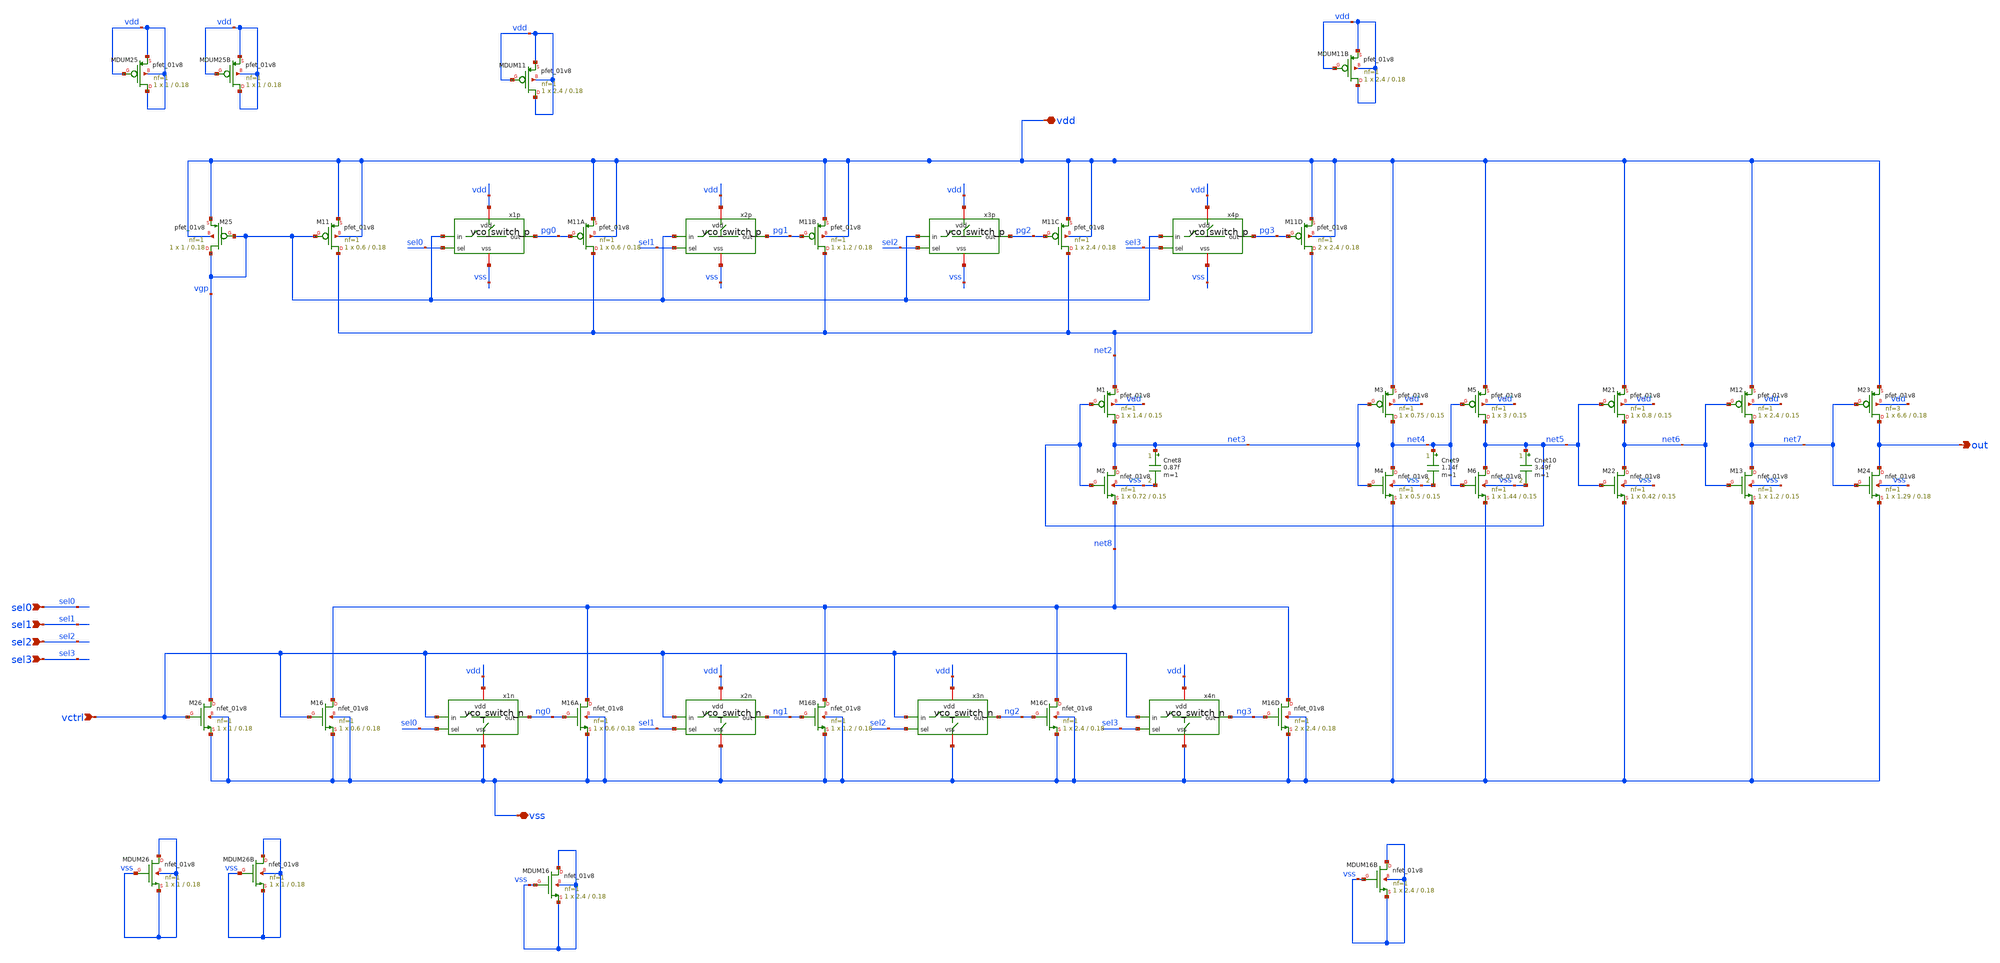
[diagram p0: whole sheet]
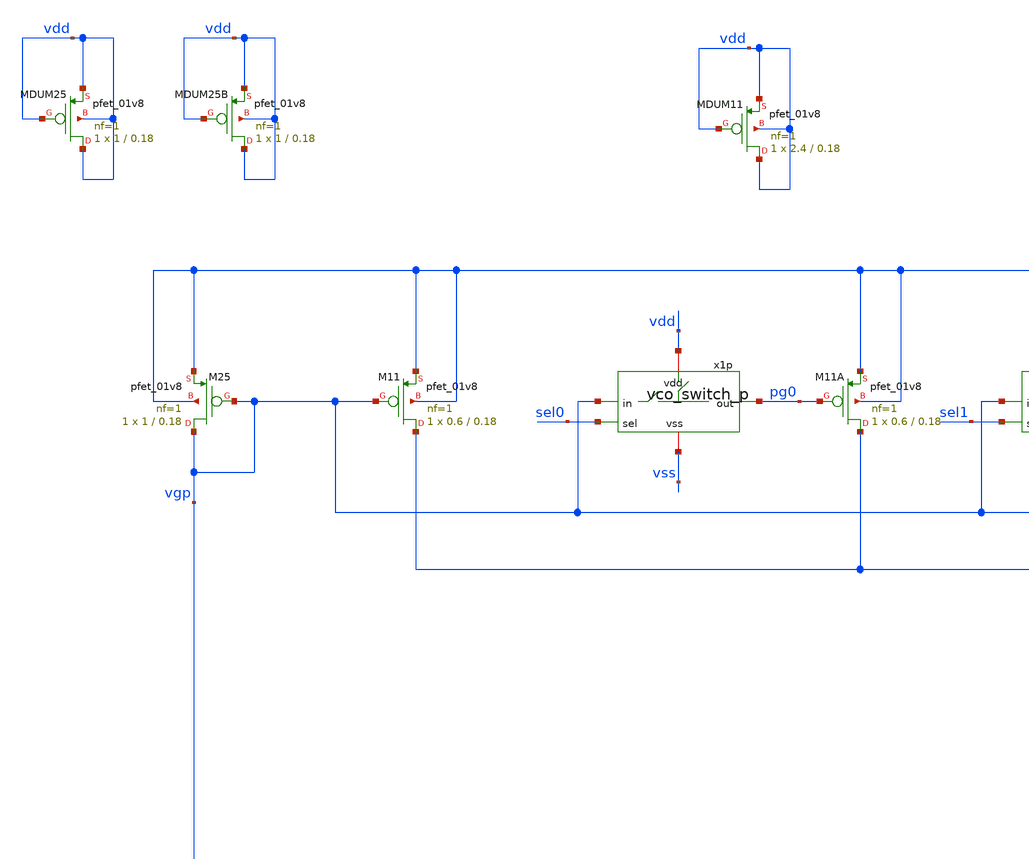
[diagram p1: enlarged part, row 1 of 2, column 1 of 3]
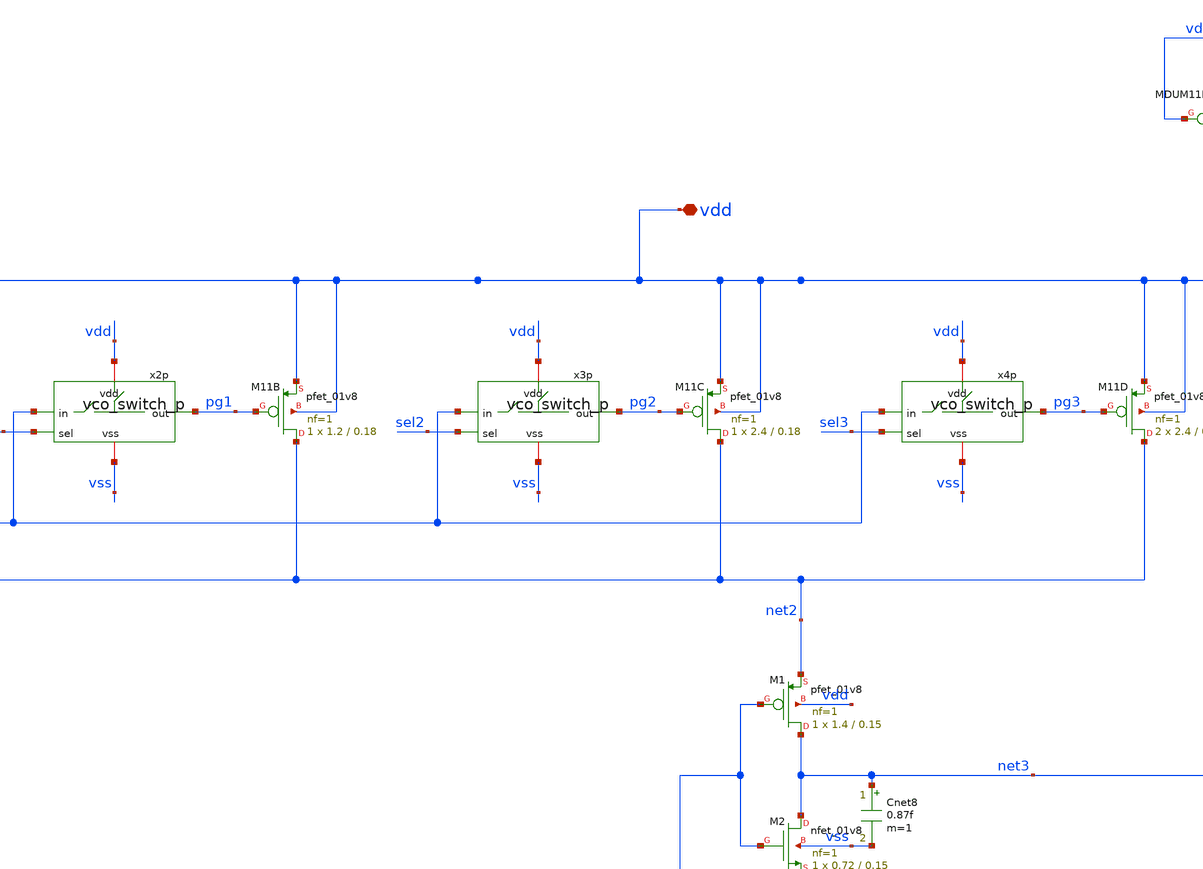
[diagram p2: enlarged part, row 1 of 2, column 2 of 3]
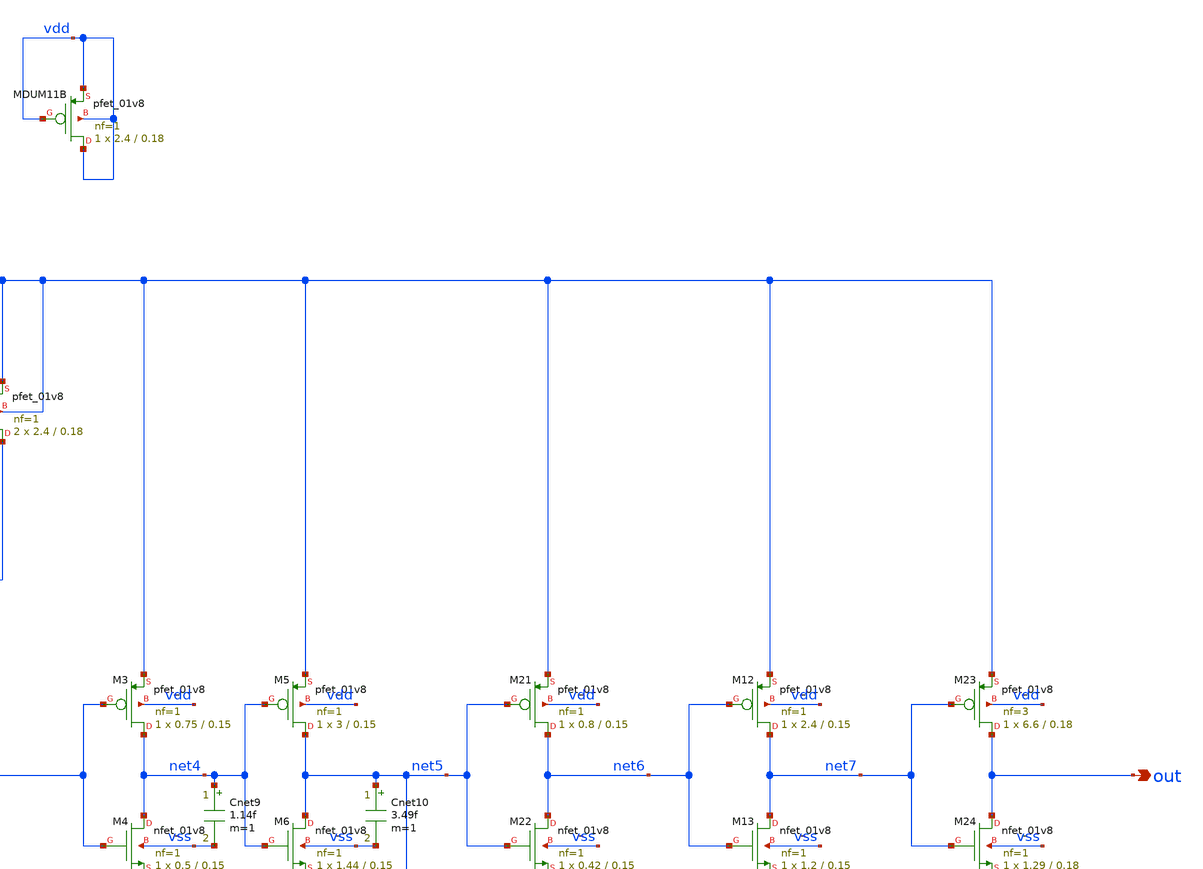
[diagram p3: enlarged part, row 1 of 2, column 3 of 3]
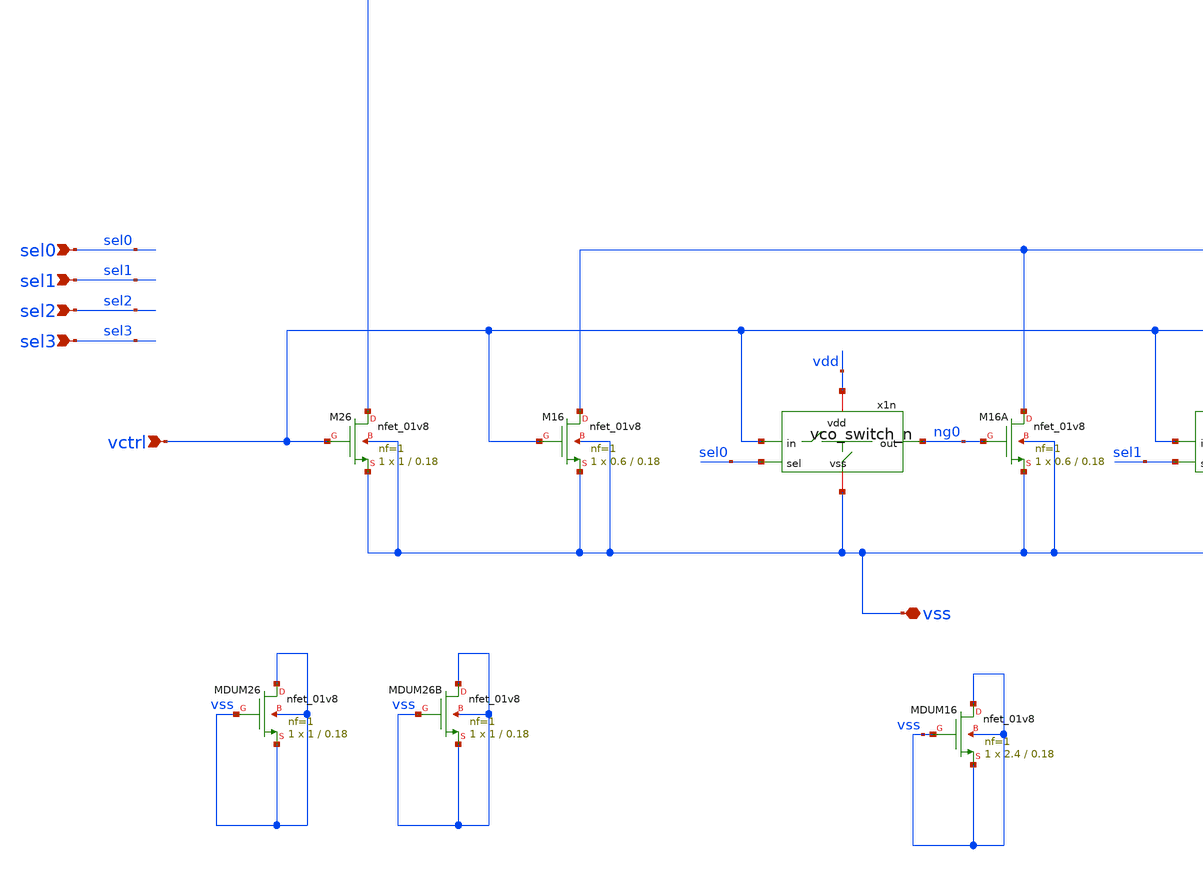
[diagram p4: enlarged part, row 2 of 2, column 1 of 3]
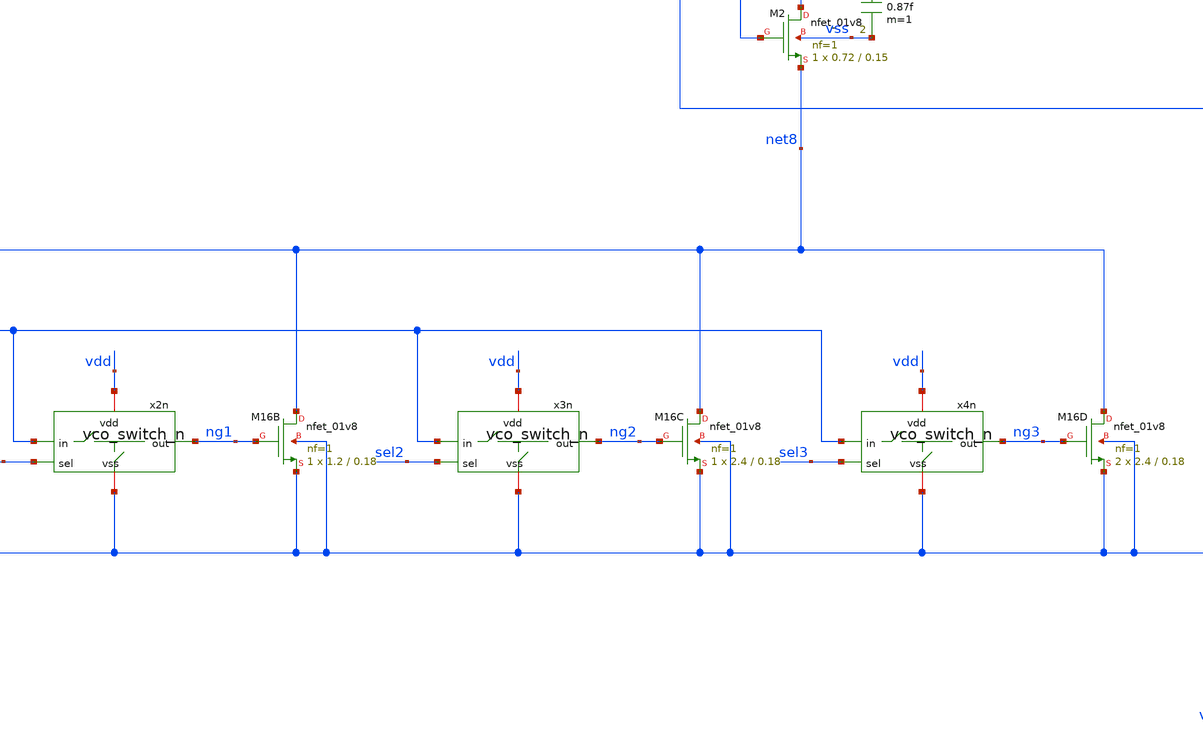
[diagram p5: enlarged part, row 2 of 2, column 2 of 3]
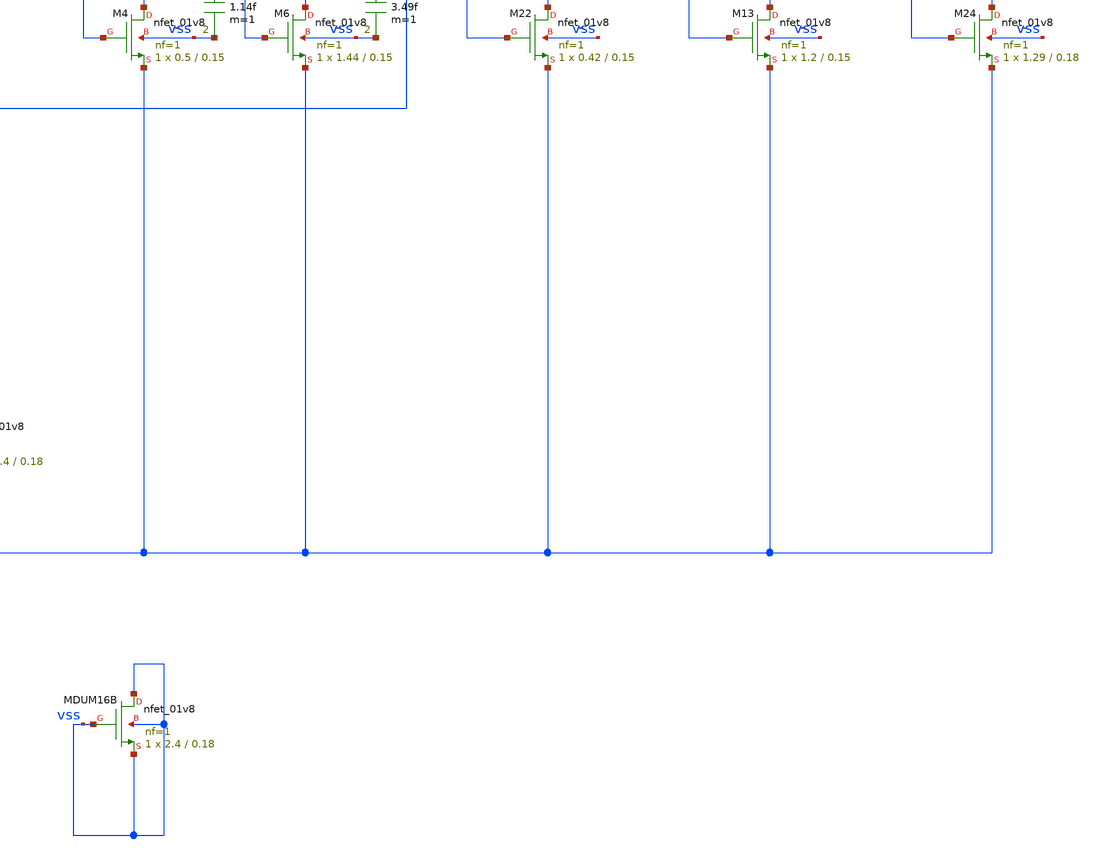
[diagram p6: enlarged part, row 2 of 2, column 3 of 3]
** sch_path: xschem/3-stage_cs-vco_dp9/3-stage_cs-vco_dp9.sch
**.subckt 3-stage_cs-vco_dp9 vdd vss out vctrl sel0 sel1 sel2 sel3
*.iopin vdd
*.iopin vss
*.opin out
*.ipin vctrl
*.ipin sel0
*.ipin sel1
*.ipin sel2
*.ipin sel3
XM25 vgp vgp vdd vdd sky130_fd_pr__pfet_01v8 L=0.18 W=1 nf=1 ad='int((nf+1)/2) * W/nf * 0.29' as='int((nf+2)/2) * W/nf * 0.29'
+ pd='2*int((nf+1)/2) * (W/nf + 0.29)' ps='2*int((nf+2)/2) * (W/nf + 0.29)' nrd='0.29 / W' nrs='0.29 / W'
+ sa=0 sb=0 sd=0 mult=1 m=1
XM26 vgp vctrl vss vss sky130_fd_pr__nfet_01v8 L=0.18 W=1 nf=1 ad='int((nf+1)/2) * W/nf * 0.29' as='int((nf+2)/2) * W/nf * 0.29'
+ pd='2*int((nf+1)/2) * (W/nf + 0.29)' ps='2*int((nf+2)/2) * (W/nf + 0.29)' nrd='0.29 / W' nrs='0.29 / W'
+ sa=0 sb=0 sd=0 mult=1 m=1
XM11C net2 pg2 vdd vdd sky130_fd_pr__pfet_01v8 L=0.18 W=2.4 nf=1 ad='int((nf+1)/2) * W/nf * 0.29' as='int((nf+2)/2) * W/nf * 0.29'
+ pd='2*int((nf+1)/2) * (W/nf + 0.29)' ps='2*int((nf+2)/2) * (W/nf + 0.29)' nrd='0.29 / W' nrs='0.29 / W'
+ sa=0 sb=0 sd=0 mult=1 m=1
XM16A net8 ng0 vss vss sky130_fd_pr__nfet_01v8 L=0.18 W=0.6 nf=1 ad='int((nf+1)/2) * W/nf * 0.29' as='int((nf+2)/2) * W/nf * 0.29'
+ pd='2*int((nf+1)/2) * (W/nf + 0.29)' ps='2*int((nf+2)/2) * (W/nf + 0.29)' nrd='0.29 / W' nrs='0.29 / W'
+ sa=0 sb=0 sd=0 mult=1 m=1
XM1 net3 net5 net2 vdd sky130_fd_pr__pfet_01v8 L=0.15 W=1.4 nf=1 ad='int((nf+1)/2) * W/nf * 0.29' as='int((nf+2)/2) * W/nf * 0.29'
+ pd='2*int((nf+1)/2) * (W/nf + 0.29)' ps='2*int((nf+2)/2) * (W/nf + 0.29)' nrd='0.29 / W' nrs='0.29 / W'
+ sa=0 sb=0 sd=0 mult=1 m=1
XM3 net4 net3 vdd vdd sky130_fd_pr__pfet_01v8 L=0.15 W=0.75 nf=1 ad='int((nf+1)/2) * W/nf * 0.29' as='int((nf+2)/2) * W/nf * 0.29'
+ pd='2*int((nf+1)/2) * (W/nf + 0.29)' ps='2*int((nf+2)/2) * (W/nf + 0.29)' nrd='0.29 / W' nrs='0.29 / W'
+ sa=0 sb=0 sd=0 mult=1 m=1
XM5 net5 net4 vdd vdd sky130_fd_pr__pfet_01v8 L=0.15 W=3 nf=1 ad='int((nf+1)/2) * W/nf * 0.29' as='int((nf+2)/2) * W/nf * 0.29'
+ pd='2*int((nf+1)/2) * (W/nf + 0.29)' ps='2*int((nf+2)/2) * (W/nf + 0.29)' nrd='0.29 / W' nrs='0.29 / W'
+ sa=0 sb=0 sd=0 mult=1 m=1
XM2 net3 net5 net8 vss sky130_fd_pr__nfet_01v8 L=0.15 W=0.72 nf=1 ad='int((nf+1)/2) * W/nf * 0.29' as='int((nf+2)/2) * W/nf * 0.29'
+ pd='2*int((nf+1)/2) * (W/nf + 0.29)' ps='2*int((nf+2)/2) * (W/nf + 0.29)' nrd='0.29 / W' nrs='0.29 / W'
+ sa=0 sb=0 sd=0 mult=1 m=1
XM4 net4 net3 vss vss sky130_fd_pr__nfet_01v8 L=0.15 W=0.5 nf=1 ad='int((nf+1)/2) * W/nf * 0.29' as='int((nf+2)/2) * W/nf * 0.29'
+ pd='2*int((nf+1)/2) * (W/nf + 0.29)' ps='2*int((nf+2)/2) * (W/nf + 0.29)' nrd='0.29 / W' nrs='0.29 / W'
+ sa=0 sb=0 sd=0 mult=1 m=1
XM6 net5 net4 vss vss sky130_fd_pr__nfet_01v8 L=0.15 W=1.44 nf=1 ad='int((nf+1)/2) * W/nf * 0.29' as='int((nf+2)/2) * W/nf * 0.29'
+ pd='2*int((nf+1)/2) * (W/nf + 0.29)' ps='2*int((nf+2)/2) * (W/nf + 0.29)' nrd='0.29 / W' nrs='0.29 / W'
+ sa=0 sb=0 sd=0 mult=1 m=1
XM21 net6 net5 vdd vdd sky130_fd_pr__pfet_01v8 L=0.15 W=0.8 nf=1 ad='int((nf+1)/2) * W/nf * 0.29' as='int((nf+2)/2) * W/nf * 0.29'
+ pd='2*int((nf+1)/2) * (W/nf + 0.29)' ps='2*int((nf+2)/2) * (W/nf + 0.29)' nrd='0.29 / W' nrs='0.29 / W'
+ sa=0 sb=0 sd=0 mult=1 m=1
XM22 net6 net5 vss vss sky130_fd_pr__nfet_01v8 L=0.15 W=0.42 nf=1 ad='int((nf+1)/2) * W/nf * 0.29' as='int((nf+2)/2) * W/nf * 0.29'
+ pd='2*int((nf+1)/2) * (W/nf + 0.29)' ps='2*int((nf+2)/2) * (W/nf + 0.29)' nrd='0.29 / W' nrs='0.29 / W'
+ sa=0 sb=0 sd=0 mult=1 m=1
XM23 out net7 vdd vdd sky130_fd_pr__pfet_01v8 L=0.18 W=6.6 nf=3 ad='int((nf+1)/2) * W/nf * 0.29' as='int((nf+2)/2) * W/nf * 0.29'
+ pd='2*int((nf+1)/2) * (W/nf + 0.29)' ps='2*int((nf+2)/2) * (W/nf + 0.29)' nrd='0.29 / W' nrs='0.29 / W'
+ sa=0 sb=0 sd=0 mult=1 m=1
XM24 out net7 vss vss sky130_fd_pr__nfet_01v8 L=0.18 W=1.29 nf=1 ad='int((nf+1)/2) * W/nf * 0.29' as='int((nf+2)/2) * W/nf * 0.29'
+ pd='2*int((nf+1)/2) * (W/nf + 0.29)' ps='2*int((nf+2)/2) * (W/nf + 0.29)' nrd='0.29 / W' nrs='0.29 / W'
+ sa=0 sb=0 sd=0 mult=1 m=1
XM12 net7 net6 vdd vdd sky130_fd_pr__pfet_01v8 L=0.15 W=2.4 nf=1 ad='int((nf+1)/2) * W/nf * 0.29' as='int((nf+2)/2) * W/nf * 0.29'
+ pd='2*int((nf+1)/2) * (W/nf + 0.29)' ps='2*int((nf+2)/2) * (W/nf + 0.29)' nrd='0.29 / W' nrs='0.29 / W'
+ sa=0 sb=0 sd=0 mult=1 m=1
XM13 net7 net6 vss vss sky130_fd_pr__nfet_01v8 L=0.15 W=1.2 nf=1 ad='int((nf+1)/2) * W/nf * 0.29' as='int((nf+2)/2) * W/nf * 0.29'
+ pd='2*int((nf+1)/2) * (W/nf + 0.29)' ps='2*int((nf+2)/2) * (W/nf + 0.29)' nrd='0.29 / W' nrs='0.29 / W'
+ sa=0 sb=0 sd=0 mult=1 m=1
XMDUM16B vss vss vss vss sky130_fd_pr__nfet_01v8 L=0.18 W=2.4 nf=1 ad='int((nf+1)/2) * W/nf * 0.29' as='int((nf+2)/2) * W/nf * 0.29'
+ pd='2*int((nf+1)/2) * (W/nf + 0.29)' ps='2*int((nf+2)/2) * (W/nf + 0.29)' nrd='0.29 / W' nrs='0.29 / W'
+ sa=0 sb=0 sd=0 mult=1 m=1
XMDUM16 vss vss vss vss sky130_fd_pr__nfet_01v8 L=0.18 W=2.4 nf=1 ad='int((nf+1)/2) * W/nf * 0.29' as='int((nf+2)/2) * W/nf * 0.29'
+ pd='2*int((nf+1)/2) * (W/nf + 0.29)' ps='2*int((nf+2)/2) * (W/nf + 0.29)' nrd='0.29 / W' nrs='0.29 / W'
+ sa=0 sb=0 sd=0 mult=1 m=1
XMDUM26 vss vss vss vss sky130_fd_pr__nfet_01v8 L=0.18 W=1 nf=1 ad='int((nf+1)/2) * W/nf * 0.29' as='int((nf+2)/2) * W/nf * 0.29'
+ pd='2*int((nf+1)/2) * (W/nf + 0.29)' ps='2*int((nf+2)/2) * (W/nf + 0.29)' nrd='0.29 / W' nrs='0.29 / W'
+ sa=0 sb=0 sd=0 mult=1 m=1
XMDUM11B vdd vdd vdd vdd sky130_fd_pr__pfet_01v8 L=0.18 W=2.4 nf=1 ad='int((nf+1)/2) * W/nf * 0.29' as='int((nf+2)/2) * W/nf * 0.29'
+ pd='2*int((nf+1)/2) * (W/nf + 0.29)' ps='2*int((nf+2)/2) * (W/nf + 0.29)' nrd='0.29 / W' nrs='0.29 / W'
+ sa=0 sb=0 sd=0 mult=1 m=1
XMDUM11 vdd vdd vdd vdd sky130_fd_pr__pfet_01v8 L=0.18 W=2.4 nf=1 ad='int((nf+1)/2) * W/nf * 0.29' as='int((nf+2)/2) * W/nf * 0.29'
+ pd='2*int((nf+1)/2) * (W/nf + 0.29)' ps='2*int((nf+2)/2) * (W/nf + 0.29)' nrd='0.29 / W' nrs='0.29 / W'
+ sa=0 sb=0 sd=0 mult=1 m=1
XMDUM25 vdd vdd vdd vdd sky130_fd_pr__pfet_01v8 L=0.18 W=1 nf=1 ad='int((nf+1)/2) * W/nf * 0.29' as='int((nf+2)/2) * W/nf * 0.29'
+ pd='2*int((nf+1)/2) * (W/nf + 0.29)' ps='2*int((nf+2)/2) * (W/nf + 0.29)' nrd='0.29 / W' nrs='0.29 / W'
+ sa=0 sb=0 sd=0 mult=1 m=1
Cnet8 net3 vss 0.87f m=1
Cnet9 net4 vss 1.14f m=1
Cnet10 net5 vss 3.49f m=1
XMDUM26B vss vss vss vss sky130_fd_pr__nfet_01v8 L=0.18 W=1 nf=1 ad='int((nf+1)/2) * W/nf * 0.29' as='int((nf+2)/2) * W/nf * 0.29'
+ pd='2*int((nf+1)/2) * (W/nf + 0.29)' ps='2*int((nf+2)/2) * (W/nf + 0.29)' nrd='0.29 / W' nrs='0.29 / W'
+ sa=0 sb=0 sd=0 mult=1 m=1
XMDUM25B vdd vdd vdd vdd sky130_fd_pr__pfet_01v8 L=0.18 W=1 nf=1 ad='int((nf+1)/2) * W/nf * 0.29' as='int((nf+2)/2) * W/nf * 0.29'
+ pd='2*int((nf+1)/2) * (W/nf + 0.29)' ps='2*int((nf+2)/2) * (W/nf + 0.29)' nrd='0.29 / W' nrs='0.29 / W'
+ sa=0 sb=0 sd=0 mult=1 m=1
x1n vdd ng0 vctrl vss sel0 vco_switch_n
XM16B net8 ng1 vss vss sky130_fd_pr__nfet_01v8 L=0.18 W=1.2 nf=1 ad='int((nf+1)/2) * W/nf * 0.29' as='int((nf+2)/2) * W/nf * 0.29'
+ pd='2*int((nf+1)/2) * (W/nf + 0.29)' ps='2*int((nf+2)/2) * (W/nf + 0.29)' nrd='0.29 / W' nrs='0.29 / W'
+ sa=0 sb=0 sd=0 mult=1 m=1
x2n vdd ng1 vctrl vss sel1 vco_switch_n
XM16C net8 ng2 vss vss sky130_fd_pr__nfet_01v8 L=0.18 W=2.4 nf=1 ad='int((nf+1)/2) * W/nf * 0.29' as='int((nf+2)/2) * W/nf * 0.29'
+ pd='2*int((nf+1)/2) * (W/nf + 0.29)' ps='2*int((nf+2)/2) * (W/nf + 0.29)' nrd='0.29 / W' nrs='0.29 / W'
+ sa=0 sb=0 sd=0 mult=1 m=1
x3n vdd ng2 vctrl vss sel2 vco_switch_n
XM16D net8 ng3 vss vss sky130_fd_pr__nfet_01v8 L=0.18 W=2.4 nf=1 ad='int((nf+1)/2) * W/nf * 0.29' as='int((nf+2)/2) * W/nf * 0.29'
+ pd='2*int((nf+1)/2) * (W/nf + 0.29)' ps='2*int((nf+2)/2) * (W/nf + 0.29)' nrd='0.29 / W' nrs='0.29 / W'
+ sa=0 sb=0 sd=0 mult=2 m=2
x4n vdd ng3 vctrl vss sel3 vco_switch_n
x3p vdd pg2 vgp vss sel2 vco_switch_p
XM11D net2 pg3 vdd vdd sky130_fd_pr__pfet_01v8 L=0.18 W=2.4 nf=1 ad='int((nf+1)/2) * W/nf * 0.29' as='int((nf+2)/2) * W/nf * 0.29'
+ pd='2*int((nf+1)/2) * (W/nf + 0.29)' ps='2*int((nf+2)/2) * (W/nf + 0.29)' nrd='0.29 / W' nrs='0.29 / W'
+ sa=0 sb=0 sd=0 mult=2 m=2
x4p vdd pg3 vgp vss sel3 vco_switch_p
XM11B net2 pg1 vdd vdd sky130_fd_pr__pfet_01v8 L=0.18 W=1.2 nf=1 ad='int((nf+1)/2) * W/nf * 0.29' as='int((nf+2)/2) * W/nf * 0.29'
+ pd='2*int((nf+1)/2) * (W/nf + 0.29)' ps='2*int((nf+2)/2) * (W/nf + 0.29)' nrd='0.29 / W' nrs='0.29 / W'
+ sa=0 sb=0 sd=0 mult=1 m=1
x2p vdd pg1 vgp vss sel1 vco_switch_p
XM11A net2 pg0 vdd vdd sky130_fd_pr__pfet_01v8 L=0.18 W=0.6 nf=1 ad='int((nf+1)/2) * W/nf * 0.29' as='int((nf+2)/2) * W/nf * 0.29'
+ pd='2*int((nf+1)/2) * (W/nf + 0.29)' ps='2*int((nf+2)/2) * (W/nf + 0.29)' nrd='0.29 / W' nrs='0.29 / W'
+ sa=0 sb=0 sd=0 mult=1 m=1
x1p vdd pg0 vgp vss sel0 vco_switch_p
XM16 net8 vctrl vss vss sky130_fd_pr__nfet_01v8 L=0.18 W=0.6 nf=1 ad='int((nf+1)/2) * W/nf * 0.29' as='int((nf+2)/2) * W/nf * 0.29'
+ pd='2*int((nf+1)/2) * (W/nf + 0.29)' ps='2*int((nf+2)/2) * (W/nf + 0.29)' nrd='0.29 / W' nrs='0.29 / W'
+ sa=0 sb=0 sd=0 mult=1 m=1
XM11 net2 vgp vdd vdd sky130_fd_pr__pfet_01v8 L=0.18 W=0.6 nf=1 ad='int((nf+1)/2) * W/nf * 0.29' as='int((nf+2)/2) * W/nf * 0.29'
+ pd='2*int((nf+1)/2) * (W/nf + 0.29)' ps='2*int((nf+2)/2) * (W/nf + 0.29)' nrd='0.29 / W' nrs='0.29 / W'
+ sa=0 sb=0 sd=0 mult=1 m=1
**.ends

* expanding   symbol:  vco_switch_n.sym # of pins=5
** sym_path: xschem/3-stage_cs-vco_dp9/vco_switch_n.sym
** sch_path: xschem/3-stage_cs-vco_dp9/vco_switch_n.sch
.subckt vco_switch_n vdd out in vss sel
*.ipin in
*.ipin sel
*.opin out
*.iopin vss
*.iopin vdd
XM26 in sel out vss sky130_fd_pr__nfet_01v8 L=0.18 W=0.42 nf=1 ad='int((nf+1)/2) * W/nf * 0.29' as='int((nf+2)/2) * W/nf * 0.29'
+ pd='2*int((nf+1)/2) * (W/nf + 0.29)' ps='2*int((nf+2)/2) * (W/nf + 0.29)' nrd='0.29 / W' nrs='0.29 / W'
+ sa=0 sb=0 sd=0 mult=1 m=1
XM25 out selb in vdd sky130_fd_pr__pfet_01v8 L=0.18 W=0.72 nf=1 ad='int((nf+1)/2) * W/nf * 0.29' as='int((nf+2)/2) * W/nf * 0.29'
+ pd='2*int((nf+1)/2) * (W/nf + 0.29)' ps='2*int((nf+2)/2) * (W/nf + 0.29)' nrd='0.29 / W' nrs='0.29 / W'
+ sa=0 sb=0 sd=0 mult=1 m=1
XM1 out selb vss vss sky130_fd_pr__nfet_01v8 L=0.18 W=0.42 nf=1 ad='int((nf+1)/2) * W/nf * 0.29' as='int((nf+2)/2) * W/nf * 0.29'
+ pd='2*int((nf+1)/2) * (W/nf + 0.29)' ps='2*int((nf+2)/2) * (W/nf + 0.29)' nrd='0.29 / W' nrs='0.29 / W'
+ sa=0 sb=0 sd=0 mult=1 m=1
x1 sel vss vss vdd vdd selb sky130_fd_sc_hd__inv_1
**** begin user architecture code

.include /usr/local/share/pdk/sky130A/libs.ref/sky130_fd_sc_hd/spice/sky130_fd_sc_hd.spice

**** end user architecture code
.ends


* expanding   symbol:  vco_switch_p.sym # of pins=5
** sym_path: xschem/3-stage_cs-vco_dp9/vco_switch_p.sym
** sch_path: xschem/3-stage_cs-vco_dp9/vco_switch_p.sch
.subckt vco_switch_p vdd out in vss sel
*.ipin in
*.ipin sel
*.opin out
*.iopin vss
*.iopin vdd
XM26 in sel out vss sky130_fd_pr__nfet_01v8 L=0.18 W=0.42 nf=1 ad='int((nf+1)/2) * W/nf * 0.29' as='int((nf+2)/2) * W/nf * 0.29'
+ pd='2*int((nf+1)/2) * (W/nf + 0.29)' ps='2*int((nf+2)/2) * (W/nf + 0.29)' nrd='0.29 / W' nrs='0.29 / W'
+ sa=0 sb=0 sd=0 mult=1 m=1
XM25 out selb in vdd sky130_fd_pr__pfet_01v8 L=0.18 W=0.72 nf=1 ad='int((nf+1)/2) * W/nf * 0.29' as='int((nf+2)/2) * W/nf * 0.29'
+ pd='2*int((nf+1)/2) * (W/nf + 0.29)' ps='2*int((nf+2)/2) * (W/nf + 0.29)' nrd='0.29 / W' nrs='0.29 / W'
+ sa=0 sb=0 sd=0 mult=1 m=1
x1 sel vss vss vdd vdd selb sky130_fd_sc_hd__inv_1
XM1 vdd sel out vdd sky130_fd_pr__pfet_01v8 L=0.18 W=0.72 nf=1 ad='int((nf+1)/2) * W/nf * 0.29' as='int((nf+2)/2) * W/nf * 0.29'
+ pd='2*int((nf+1)/2) * (W/nf + 0.29)' ps='2*int((nf+2)/2) * (W/nf + 0.29)' nrd='0.29 / W' nrs='0.29 / W'
+ sa=0 sb=0 sd=0 mult=1 m=1
**** begin user architecture code

.include /usr/local/share/pdk/sky130A/libs.ref/sky130_fd_sc_hd/spice/sky130_fd_sc_hd.spice

**** end user architecture code
.ends

.end
